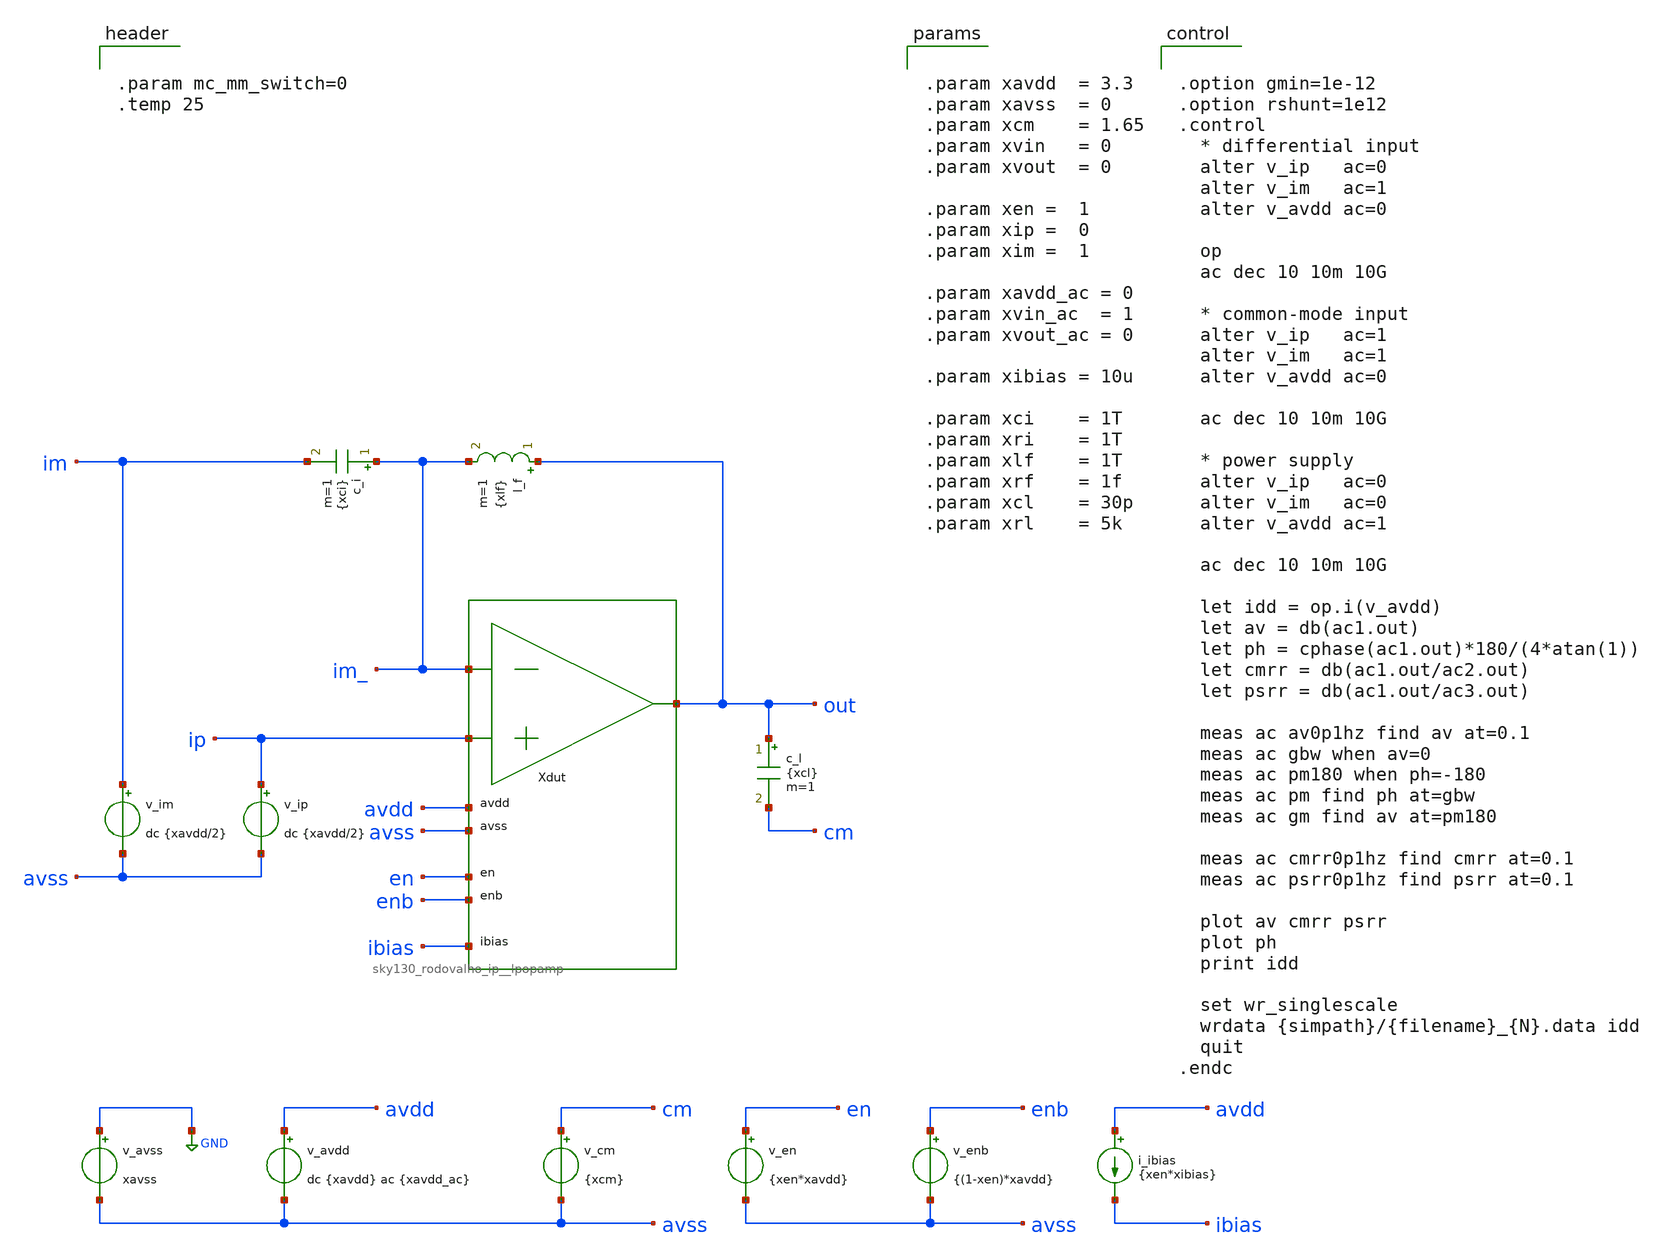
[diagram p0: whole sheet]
** sch_path: cace/tb_lpopamp_open_ac.sch
**.subckt tb_lpopamp_open_ac
Xdut im_ ip out avdd avss en enb ibias sky130_rodovalho_ip__lpopamp
v_avss GND avss xavss
v_avdd avdd avss dc {xavdd} ac {xavdd_ac}
v_en en avss {xen*xavdd}
v_enb enb avss {(1-xen)*xavdd}
i_ibias avdd ibias {xen*xibias}
c_l out cm {xcl} m=1
c_i im_ im {xci} m=1
l_f out im_ {xlf} m=1
v_cm cm avss {xcm}
v_im im avss dc {xavdd/2}
v_ip ip avss dc {xavdd/2}
**** begin user architecture code


.param mc_mm_switch=0
.temp 25




.option gmin=1e-12
.option rshunt=1e12
.control
  * differential input
  alter v_ip   ac=0
  alter v_im   ac=1
  alter v_avdd ac=0

  op
  ac dec 10 10m 10G

  * common-mode input
  alter v_ip   ac=1
  alter v_im   ac=1
  alter v_avdd ac=0

  ac dec 10 10m 10G

  * power supply
  alter v_ip   ac=0
  alter v_im   ac=0
  alter v_avdd ac=1

  ac dec 10 10m 10G

  let idd = op.i(v_avdd)
  let av = db(ac1.out)
  let ph = cphase(ac1.out)*180/(4*atan(1))
  let cmrr = db(ac1.out/ac2.out)
  let psrr = db(ac1.out/ac3.out)

  meas ac av0p1hz find av at=0.1
  meas ac gbw when av=0
  meas ac pm180 when ph=-180
  meas ac pm find ph at=gbw
  meas ac gm find av at=pm180

  meas ac cmrr0p1hz find cmrr at=0.1
  meas ac psrr0p1hz find psrr at=0.1

  plot av cmrr psrr
  plot ph
  print idd

  set wr_singlescale
  wrdata {simpath}/{filename}_{N}.data idd
  quit
.endc




.param xavdd  = 3.3
.param xavss  = 0
.param xcm    = 1.65
.param xvin   = 0
.param xvout  = 0

.param xen =  1
.param xip =  0
.param xim =  1

.param xavdd_ac = 0
.param xvin_ac  = 1
.param xvout_ac = 0

.param xibias = 10u

.param xci    = 1T
.param xri    = 1T
.param xlf    = 1T
.param xrf    = 1f
.param xcl    = 30p
.param xrl    = 5k



** opencircuitdesign pdks install
.lib $::SKYWATER_MODELS/sky130.lib.spice tt


**** end user architecture code
**.ends
.GLOBAL GND
.end
